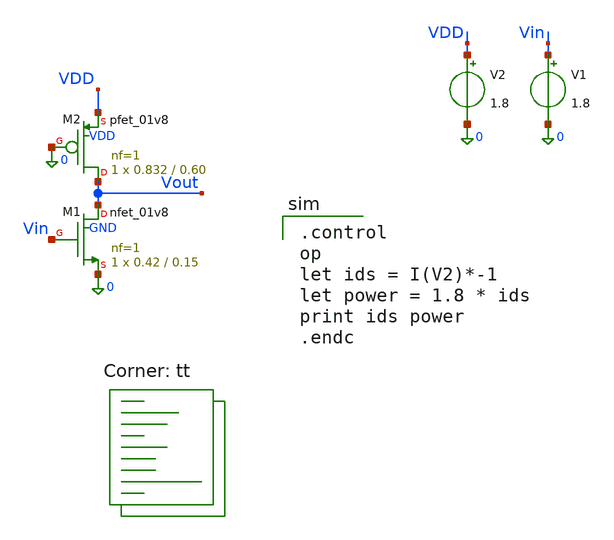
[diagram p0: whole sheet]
** sch_path: tutorial-2/source/q2c.sch
**.subckt q2c
V1 Vin 0 1.8
XM1 Vout Vin 0 GND sky130_fd_pr__nfet_01v8 L=0.15 W=0.42 nf=1 ad='int((nf+1)/2) * W/nf * 0.29' as='int((nf+2)/2) * W/nf * 0.29'
+ pd='2*int((nf+1)/2) * (W/nf + 0.29)' ps='2*int((nf+2)/2) * (W/nf + 0.29)' nrd='0.29 / W' nrs='0.29 / W'
+ sa=0 sb=0 sd=0 mult=1 m=1
XM2 Vout 0 VDD VDD sky130_fd_pr__pfet_01v8 L=0.60 W=0.832 nf=1 ad='int((nf+1)/2) * W/nf * 0.29' as='int((nf+2)/2) * W/nf * 0.29'
+ pd='2*int((nf+1)/2) * (W/nf + 0.29)' ps='2*int((nf+2)/2) * (W/nf + 0.29)' nrd='0.29 / W' nrs='0.29 / W'
+ sa=0 sb=0 sd=0 mult=1 m=1
V2 VDD 0 1.8
**** begin user architecture code
.lib $::SKYWATER_MODELS/sky130.lib.spice tt

.control
op
let ids = I(V2)*-1
let power = 1.8 * ids
print ids power
.endc

**** end user architecture code
**.ends
.end
